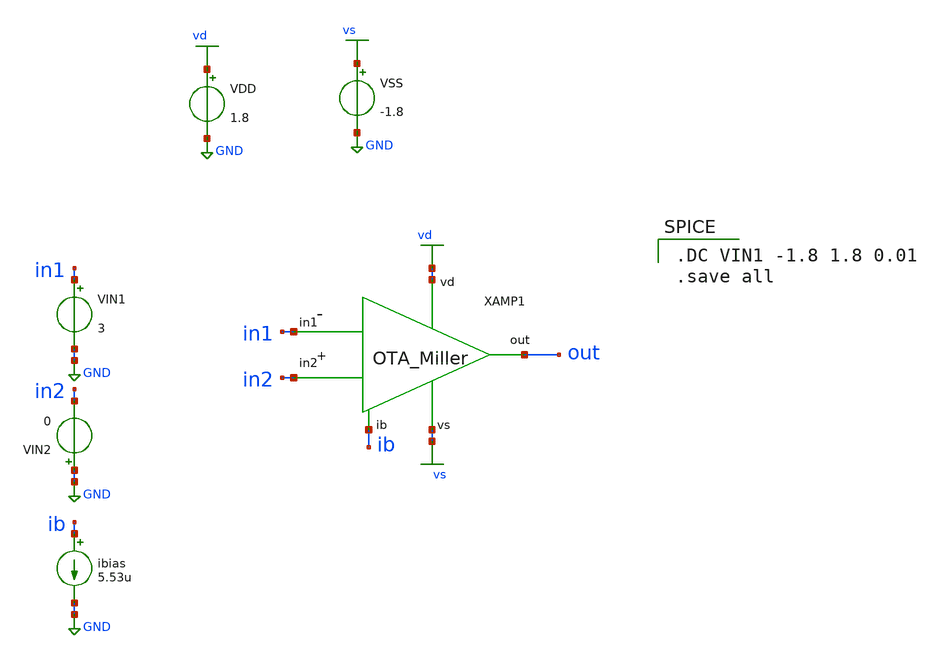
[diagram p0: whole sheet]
** sch_path: xschem/ota_tb-dc.sch
* Copyright 2020 Stefan Frederik Schippers
* Licensed under the Apache License, Version 2.0 (the "License");
* you may not use this file except in compliance with the License.
* You may obtain a copy of the License at
* https://www.apache.org/licenses/LICENSE-2.0
* Unless required by applicable law or agreed to in writing, software
* distributed under the License is distributed on an "AS IS" BASIS,
* WITHOUT WARRANTIES OR CONDITIONS OF ANY KIND, either express or implied.
* See the License for the specific language governing permissions and
* limitations under the License.
**.subckt ota_tb-dc
VIN2 GND in2 0
VIN1 in1 GND 3
ibias ib GND 5.53u
VDD vd GND 1.8
VSS vs GND -1.8
X1 vd ib out in2 in1 vs ota
**** begin user architecture code

.option wnflag=1
.lib ~/skywater/skywater-pdk/libraries/sky130_fd_pr_ngspice/latest/models/sky130.lib.spice tt


.DC VIN1 -1.8 1.8 0.01
.save all

**** end user architecture code
**.ends

* expanding   symbol:  my_projects/dpga/ota.sym # of pins=6
** sym_path: xschem/ota.sym
** sch_path: xschem/ota.sch
.subckt ota vd ib out in2 in1 vs
*.iopin vd
*.opin out
*.iopin vs
*.iopin ib
*.ipin in1
*.ipin in2
Cc net1 net4 0.5p m=1
XM4 net4 net3 vs vs sky130_fd_pr__nfet_01v8 L=1 W=0.861 nf=1 ad='int((nf+1)/2) * W/nf * 0.29' as='int((nf+2)/2) * W/nf * 0.29'
+ pd='2*int((nf+1)/2) * (W/nf + 0.29)' ps='2*int((nf+2)/2) * (W/nf + 0.29)' nrd='0.29 / W' nrs='0.29 / W'
+ sa=0 sb=0 sd=0 mult=1 m=1
XM7 net1 net4 vs vs sky130_fd_pr__nfet_01v8 L=1 W=8.61 nf=1 ad='int((nf+1)/2) * W/nf * 0.29' as='int((nf+2)/2) * W/nf * 0.29'
+ pd='2*int((nf+1)/2) * (W/nf + 0.29)' ps='2*int((nf+2)/2) * (W/nf + 0.29)' nrd='0.29 / W' nrs='0.29 / W'
+ sa=0 sb=0 sd=0 mult=1 m=1
XM5 ib ib vd vd sky130_fd_pr__pfet_01v8 L=1 W=5.85 nf=1 ad='int((nf+1)/2) * W/nf * 0.29' as='int((nf+2)/2) * W/nf * 0.29'
+ pd='2*int((nf+1)/2) * (W/nf + 0.29)' ps='2*int((nf+2)/2) * (W/nf + 0.29)' nrd='0.29 / W' nrs='0.29 / W'
+ sa=0 sb=0 sd=0 mult=1 m=1
XM6 net2 ib vd vd sky130_fd_pr__pfet_01v8 L=1 W=5.85 nf=1 ad='int((nf+1)/2) * W/nf * 0.29' as='int((nf+2)/2) * W/nf * 0.29'
+ pd='2*int((nf+1)/2) * (W/nf + 0.29)' ps='2*int((nf+2)/2) * (W/nf + 0.29)' nrd='0.29 / W' nrs='0.29 / W'
+ sa=0 sb=0 sd=0 mult=1 m=1
XM8 net1 ib vd vd sky130_fd_pr__pfet_01v8 L=1 W=29.3 nf=1 ad='int((nf+1)/2) * W/nf * 0.29' as='int((nf+2)/2) * W/nf * 0.29'
+ pd='2*int((nf+1)/2) * (W/nf + 0.29)' ps='2*int((nf+2)/2) * (W/nf + 0.29)' nrd='0.29 / W' nrs='0.29 / W'
+ sa=0 sb=0 sd=0 mult=1 m=1
XM10 out ib vd vd sky130_fd_pr__pfet_01v8 L=1 W=5.85 nf=1 ad='int((nf+1)/2) * W/nf * 0.29' as='int((nf+2)/2) * W/nf * 0.29'
+ pd='2*int((nf+1)/2) * (W/nf + 0.29)' ps='2*int((nf+2)/2) * (W/nf + 0.29)' nrd='0.29 / W' nrs='0.29 / W'
+ sa=0 sb=0 sd=0 mult=1 m=1
XM9 vs net1 out out sky130_fd_pr__pfet_01v8 L=1 W=5.85 nf=1 ad='int((nf+1)/2) * W/nf * 0.29' as='int((nf+2)/2) * W/nf * 0.29'
+ pd='2*int((nf+1)/2) * (W/nf + 0.29)' ps='2*int((nf+2)/2) * (W/nf + 0.29)' nrd='0.29 / W' nrs='0.29 / W'
+ sa=0 sb=0 sd=0 mult=1 m=1
XM1 net3 in1 net2 net2 sky130_fd_pr__pfet_01v8 L=1 W=2.93 nf=1 ad='int((nf+1)/2) * W/nf * 0.29' as='int((nf+2)/2) * W/nf * 0.29'
+ pd='2*int((nf+1)/2) * (W/nf + 0.29)' ps='2*int((nf+2)/2) * (W/nf + 0.29)' nrd='0.29 / W' nrs='0.29 / W'
+ sa=0 sb=0 sd=0 mult=1 m=1
XM2 net4 in2 net2 net2 sky130_fd_pr__pfet_01v8 L=1 W=2.93 nf=1 ad='int((nf+1)/2) * W/nf * 0.29' as='int((nf+2)/2) * W/nf * 0.29'
+ pd='2*int((nf+1)/2) * (W/nf + 0.29)' ps='2*int((nf+2)/2) * (W/nf + 0.29)' nrd='0.29 / W' nrs='0.29 / W'
+ sa=0 sb=0 sd=0 mult=1 m=1
XM3 net3 net3 vs vs sky130_fd_pr__nfet_01v8 L=1 W=0.861 nf=1 ad='int((nf+1)/2) * W/nf * 0.29' as='int((nf+2)/2) * W/nf * 0.29'
+ pd='2*int((nf+1)/2) * (W/nf + 0.29)' ps='2*int((nf+2)/2) * (W/nf + 0.29)' nrd='0.29 / W' nrs='0.29 / W'
+ sa=0 sb=0 sd=0 mult=1 m=1
.ends

.GLOBAL GND
.GLOBAL vd
.GLOBAL vs
.end
